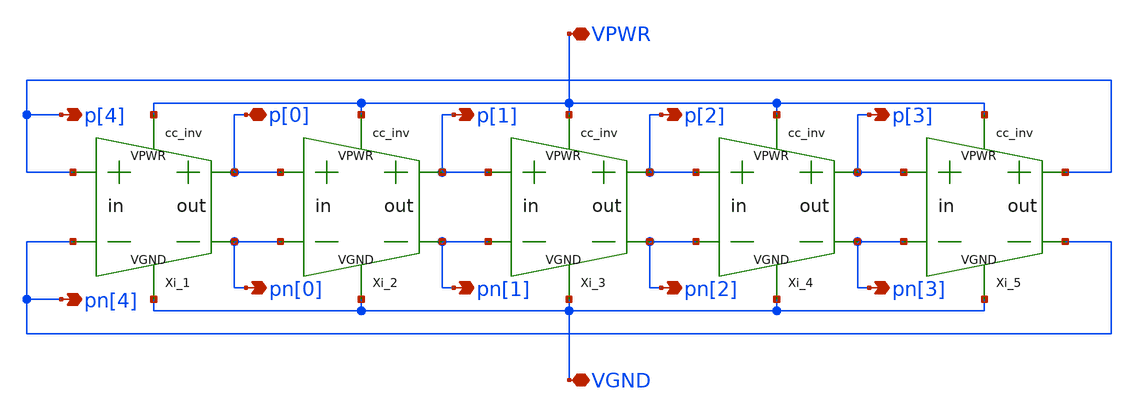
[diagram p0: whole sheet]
** sch_path: xschem/lib/ring_osc.sch
**.subckt ring_osc VPWR VGND pn[0] p[0] pn[1] p[1] p[2] p[3] p[4] pn[2] pn[3] pn[4]
*.iopin VPWR
*.iopin VGND
*.opin pn[0]
*.iopin p[0]
*.opin pn[1]
*.opin p[1]
*.opin p[2]
*.opin p[3]
*.opin p[4]
*.opin pn[2]
*.opin pn[3]
*.opin pn[4]
Xi_1 p[4] pn[4] VPWR VGND p[0] pn[0] cc_inv L12="L12" Wp12="Wp12" Wn12="Wn12" L34="L34" Wp34="Wp34"
+ Wn34="Wn34"
Xi_2 p[0] pn[0] VPWR VGND p[1] pn[1] cc_inv L12="L12" Wp12="Wp12" Wn12="Wn12" L34="L34" Wp34="Wp34"
+ Wn34="Wn34"
Xi_3 p[1] pn[1] VPWR VGND p[2] pn[2] cc_inv L12="L12" Wp12="Wp12" Wn12="Wn12" L34="L34" Wp34="Wp34"
+ Wn34="Wn34"
Xi_4 p[2] pn[2] VPWR VGND p[3] pn[3] cc_inv L12="L12" Wp12="Wp12" Wn12="Wn12" L34="L34" Wp34="Wp34"
+ Wn34="Wn34"
Xi_5 p[3] pn[3] VPWR VGND p[4] pn[4] cc_inv L12="L12" Wp12="Wp12" Wn12="Wn12" L34="L34" Wp34="Wp34"
+ Wn34="Wn34"
**.ends
.end
